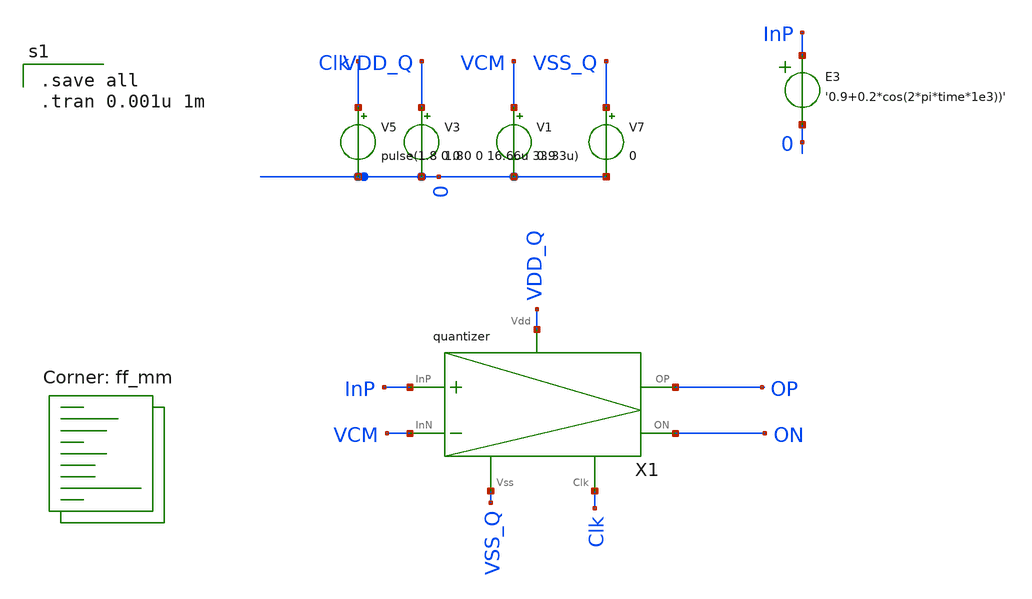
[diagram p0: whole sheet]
** sch_path: xschem/tb_quantizer.sch
**.subckt tb_quantizer
X1 VSS_Q Clk VDD_Q InP VCM OP ON quantizer
V3 VDD_Q 0 1.8
V5 Clk 0 pulse(1.8 0 0 0 0 16.66u 33.33u)
V7 VSS_Q 0 0
V1 VCM 0 0.9
E3 InP 0 VOL=' '0.9+0.2*cos(2*pi*time*1e3))' '
**** begin user architecture code
.lib $::SKYWATER_MODELS/sky130.lib.spice ff_mm

.save all
.tran 0.001u 1m


**** end user architecture code
**.ends

* expanding   symbol:  quantizer.sym # of pins=7
** sym_path: xschem/quantizer.sym
** sch_path: xschem/quantizer.sch
.subckt quantizer Vss Clk Vdd InP InN OP ON
*.iopin Vss
*.iopin Vdd
*.iopin Clk
*.ipin InP
*.ipin InN
*.iopin ON
*.iopin OP
XM29 nodeA1 InP net1 Vss sky130_fd_pr__nfet_01v8 L=1 W=2 nf=3 ad='int((nf+1)/2) * W/nf * 0.29' as='int((nf+2)/2) * W/nf * 0.29'
+ pd='2*int((nf+1)/2) * (W/nf + 0.29)' ps='2*int((nf+2)/2) * (W/nf + 0.29)' nrd='0.29 / W' nrs='0.29 / W'
+ sa=0 sb=0 sd=0 mult=1 m=1
XM30 NodeA2 InN net1 Vss sky130_fd_pr__nfet_01v8 L=1 W=2 nf=3 ad='int((nf+1)/2) * W/nf * 0.29' as='int((nf+2)/2) * W/nf * 0.29'
+ pd='2*int((nf+1)/2) * (W/nf + 0.29)' ps='2*int((nf+2)/2) * (W/nf + 0.29)' nrd='0.29 / W' nrs='0.29 / W'
+ sa=0 sb=0 sd=0 mult=1 m=1
XM31 OP ON NodeA2 Vss sky130_fd_pr__nfet_01v8 L=1 W=2 nf=1 ad='int((nf+1)/2) * W/nf * 0.29' as='int((nf+2)/2) * W/nf * 0.29'
+ pd='2*int((nf+1)/2) * (W/nf + 0.29)' ps='2*int((nf+2)/2) * (W/nf + 0.29)' nrd='0.29 / W' nrs='0.29 / W'
+ sa=0 sb=0 sd=0 mult=1 m=1
XM32 ON OP nodeA1 Vss sky130_fd_pr__nfet_01v8 L=1 W=2 nf=1 ad='int((nf+1)/2) * W/nf * 0.29' as='int((nf+2)/2) * W/nf * 0.29'
+ pd='2*int((nf+1)/2) * (W/nf + 0.29)' ps='2*int((nf+2)/2) * (W/nf + 0.29)' nrd='0.29 / W' nrs='0.29 / W'
+ sa=0 sb=0 sd=0 mult=1 m=1
XM34 OP ON Vdd Vdd sky130_fd_pr__pfet_01v8 L=1 W=4 nf=1 ad='int((nf+1)/2) * W/nf * 0.29' as='int((nf+2)/2) * W/nf * 0.29'
+ pd='2*int((nf+1)/2) * (W/nf + 0.29)' ps='2*int((nf+2)/2) * (W/nf + 0.29)' nrd='0.29 / W' nrs='0.29 / W'
+ sa=0 sb=0 sd=0 mult=1 m=1
XM35 ON OP Vdd Vdd sky130_fd_pr__pfet_01v8 L=1 W=4 nf=1 ad='int((nf+1)/2) * W/nf * 0.29' as='int((nf+2)/2) * W/nf * 0.29'
+ pd='2*int((nf+1)/2) * (W/nf + 0.29)' ps='2*int((nf+2)/2) * (W/nf + 0.29)' nrd='0.29 / W' nrs='0.29 / W'
+ sa=0 sb=0 sd=0 mult=1 m=1
XM36 ON Clk Vdd Vdd sky130_fd_pr__pfet_01v8 L=1 W=4 nf=4 ad='int((nf+1)/2) * W/nf * 0.29' as='int((nf+2)/2) * W/nf * 0.29'
+ pd='2*int((nf+1)/2) * (W/nf + 0.29)' ps='2*int((nf+2)/2) * (W/nf + 0.29)' nrd='0.29 / W' nrs='0.29 / W'
+ sa=0 sb=0 sd=0 mult=1 m=1
XM37 nodeA1 Clk Vdd Vdd sky130_fd_pr__pfet_01v8 L=1 W=4 nf=4 ad='int((nf+1)/2) * W/nf * 0.29' as='int((nf+2)/2) * W/nf * 0.29'
+ pd='2*int((nf+1)/2) * (W/nf + 0.29)' ps='2*int((nf+2)/2) * (W/nf + 0.29)' nrd='0.29 / W' nrs='0.29 / W'
+ sa=0 sb=0 sd=0 mult=1 m=1
XM38 OP Clk Vdd Vdd sky130_fd_pr__pfet_01v8 L=1 W=4 nf=4 ad='int((nf+1)/2) * W/nf * 0.29' as='int((nf+2)/2) * W/nf * 0.29'
+ pd='2*int((nf+1)/2) * (W/nf + 0.29)' ps='2*int((nf+2)/2) * (W/nf + 0.29)' nrd='0.29 / W' nrs='0.29 / W'
+ sa=0 sb=0 sd=0 mult=1 m=1
XM39 NodeA2 Clk Vdd Vdd sky130_fd_pr__pfet_01v8 L=1 W=4 nf=4 ad='int((nf+1)/2) * W/nf * 0.29' as='int((nf+2)/2) * W/nf * 0.29'
+ pd='2*int((nf+1)/2) * (W/nf + 0.29)' ps='2*int((nf+2)/2) * (W/nf + 0.29)' nrd='0.29 / W' nrs='0.29 / W'
+ sa=0 sb=0 sd=0 mult=1 m=1
XM1 OP Vss Vss Vss sky130_fd_pr__nfet_01v8 L=1 W=2 nf=5 ad='int((nf+1)/2) * W/nf * 0.29' as='int((nf+2)/2) * W/nf * 0.29'
+ pd='2*int((nf+1)/2) * (W/nf + 0.29)' ps='2*int((nf+2)/2) * (W/nf + 0.29)' nrd='0.29 / W' nrs='0.29 / W'
+ sa=0 sb=0 sd=0 mult=1 m=1
XM2 ON Vss Vss Vss sky130_fd_pr__nfet_01v8 L=1 W=2 nf=5 ad='int((nf+1)/2) * W/nf * 0.29' as='int((nf+2)/2) * W/nf * 0.29'
+ pd='2*int((nf+1)/2) * (W/nf + 0.29)' ps='2*int((nf+2)/2) * (W/nf + 0.29)' nrd='0.29 / W' nrs='0.29 / W'
+ sa=0 sb=0 sd=0 mult=1 m=1
XM3 ON Vdd Vdd Vdd sky130_fd_pr__pfet_01v8 L=1 W=4 nf=1 ad='int((nf+1)/2) * W/nf * 0.29' as='int((nf+2)/2) * W/nf * 0.29'
+ pd='2*int((nf+1)/2) * (W/nf + 0.29)' ps='2*int((nf+2)/2) * (W/nf + 0.29)' nrd='0.29 / W' nrs='0.29 / W'
+ sa=0 sb=0 sd=0 mult=1 m=1
XM4 OP Vdd Vdd Vdd sky130_fd_pr__pfet_01v8 L=1 W=4 nf=1 ad='int((nf+1)/2) * W/nf * 0.29' as='int((nf+2)/2) * W/nf * 0.29'
+ pd='2*int((nf+1)/2) * (W/nf + 0.29)' ps='2*int((nf+2)/2) * (W/nf + 0.29)' nrd='0.29 / W' nrs='0.29 / W'
+ sa=0 sb=0 sd=0 mult=1 m=1
XM5 net1 Clk Vss Vss sky130_fd_pr__nfet_01v8 L=1 W=2 nf=4 ad='int((nf+1)/2) * W/nf * 0.29' as='int((nf+2)/2) * W/nf * 0.29'
+ pd='2*int((nf+1)/2) * (W/nf + 0.29)' ps='2*int((nf+2)/2) * (W/nf + 0.29)' nrd='0.29 / W' nrs='0.29 / W'
+ sa=0 sb=0 sd=0 mult=1 m=1
XM6 nodeA1 Vdd Vdd Vdd sky130_fd_pr__pfet_01v8 L=1 W=4 nf=1 ad='int((nf+1)/2) * W/nf * 0.29' as='int((nf+2)/2) * W/nf * 0.29'
+ pd='2*int((nf+1)/2) * (W/nf + 0.29)' ps='2*int((nf+2)/2) * (W/nf + 0.29)' nrd='0.29 / W' nrs='0.29 / W'
+ sa=0 sb=0 sd=0 mult=1 m=1
XM7 NodeA2 Vdd Vdd Vdd sky130_fd_pr__pfet_01v8 L=1 W=4 nf=1 ad='int((nf+1)/2) * W/nf * 0.29' as='int((nf+2)/2) * W/nf * 0.29'
+ pd='2*int((nf+1)/2) * (W/nf + 0.29)' ps='2*int((nf+2)/2) * (W/nf + 0.29)' nrd='0.29 / W' nrs='0.29 / W'
+ sa=0 sb=0 sd=0 mult=1 m=1
C4 Vdd NodeA2 3.10f m=1
C3 Vdd nodeA1 3.17f m=1
C1 Vdd OP 3.37f m=1
C5 Vdd ON 3.45f m=1
C2 ON OP 4.89f m=1
C7 Vdd Clk 15.64f m=1
C6 OP Clk 2.62f m=1
C0 ON Clk 2.30f m=1
.ends

.end
